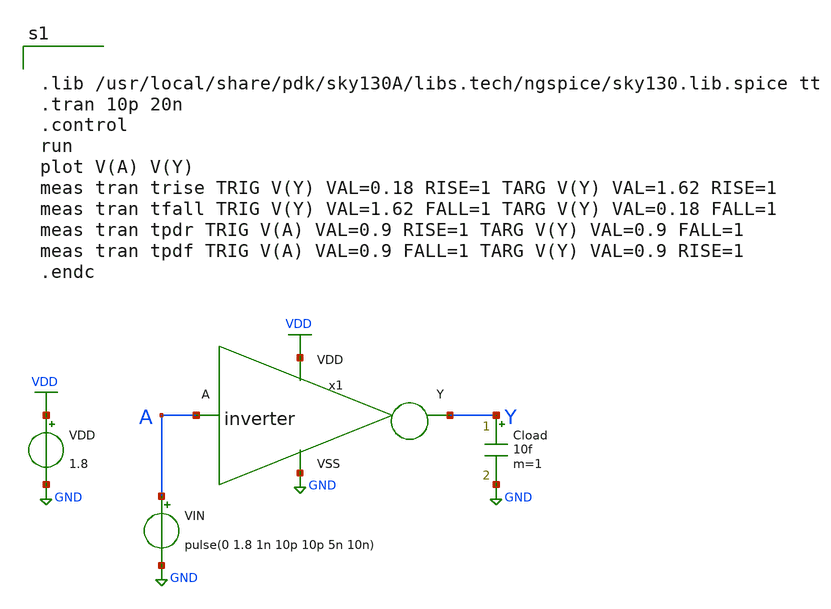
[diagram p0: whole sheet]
** sch_path: inverter/design_circuit/tran_inverter.sch
**.subckt tran_inverter
VIN A GND pulse(0 1.8 1n 10p 10p 5n 10n)
x1 A Y VDD GND inverter
Cload Y GND 10f m=1
VDD VDD GND 1.8
**** begin user architecture code


.lib /usr/local/share/pdk/sky130A/libs.tech/ngspice/sky130.lib.spice tt
.tran 10p 20n
.control
run
plot V(A) V(Y)
meas tran trise TRIG V(Y) VAL=0.18 RISE=1 TARG V(Y) VAL=1.62 RISE=1
meas tran tfall TRIG V(Y) VAL=1.62 FALL=1 TARG V(Y) VAL=0.18 FALL=1
meas tran tpdr TRIG V(A) VAL=0.9 RISE=1 TARG V(Y) VAL=0.9 FALL=1
meas tran tpdf TRIG V(A) VAL=0.9 FALL=1 TARG V(Y) VAL=0.9 RISE=1
.endc


**** end user architecture code
**.ends
.GLOBAL GND
.GLOBAL VDD
.end
